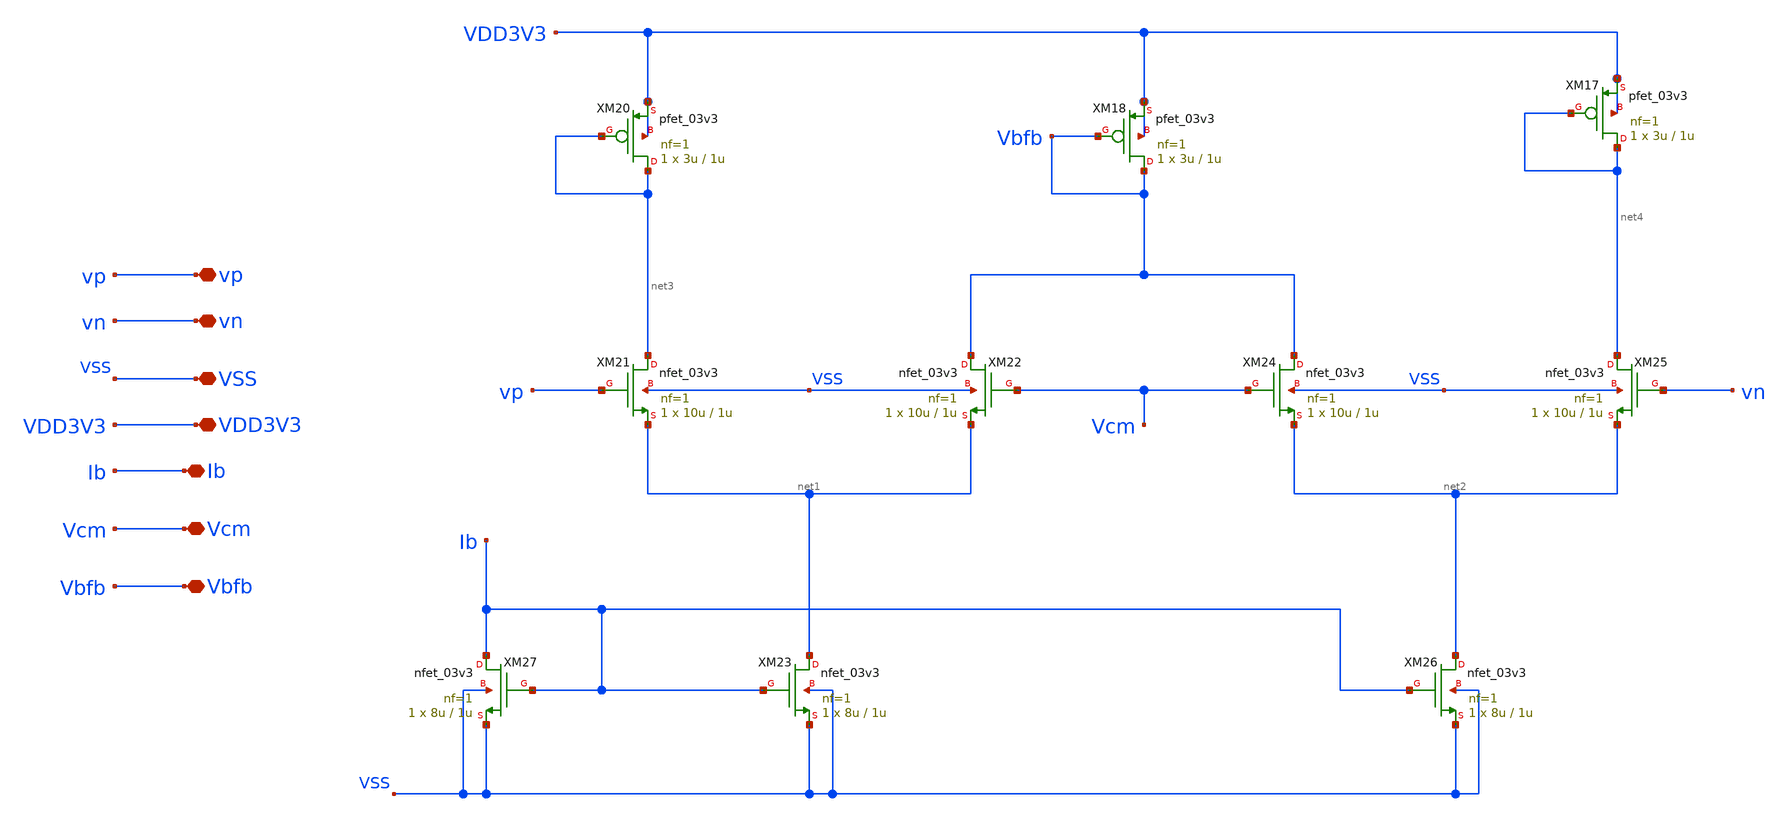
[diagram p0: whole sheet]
** sch_path: designs/libs/core_pga/folded_cascode/cmfb.sch
**.subckt cmfb VSS VDD3V3 Ib Vcm Vbfb vp vn
*.iopin VSS
*.iopin VDD3V3
*.iopin Ib
*.iopin Vcm
*.iopin Vbfb
*.iopin vp
*.iopin vn
XM20 net3 net3 VDD3V3 VDD3V3 pfet_03v3 L=1u W=3u nf=1 ad='int((nf+1)/2) * W/nf * 0.18u' as='int((nf+2)/2) * W/nf * 0.18u'
+ pd='2*int((nf+1)/2) * (W/nf + 0.18u)' ps='2*int((nf+2)/2) * (W/nf + 0.18u)' nrd='0.18u / W' nrs='0.18u / W'
+ sa=0 sb=0 sd=0 m=1
XM21 net3 vp net1 VSS nfet_03v3 L=1u W=10u nf=1 ad='int((nf+1)/2) * W/nf * 0.18u' as='int((nf+2)/2) * W/nf * 0.18u'
+ pd='2*int((nf+1)/2) * (W/nf + 0.18u)' ps='2*int((nf+2)/2) * (W/nf + 0.18u)' nrd='0.18u / W' nrs='0.18u / W'
+ sa=0 sb=0 sd=0 m=1
XM22 Vbfb Vcm net1 VSS nfet_03v3 L=1u W=10u nf=1 ad='int((nf+1)/2) * W/nf * 0.18u' as='int((nf+2)/2) * W/nf * 0.18u'
+ pd='2*int((nf+1)/2) * (W/nf + 0.18u)' ps='2*int((nf+2)/2) * (W/nf + 0.18u)' nrd='0.18u / W' nrs='0.18u / W'
+ sa=0 sb=0 sd=0 m=1
XM23 net1 Ib VSS VSS nfet_03v3 L=1u W=8u nf=1 ad='int((nf+1)/2) * W/nf * 0.18u' as='int((nf+2)/2) * W/nf * 0.18u'
+ pd='2*int((nf+1)/2) * (W/nf + 0.18u)' ps='2*int((nf+2)/2) * (W/nf + 0.18u)' nrd='0.18u / W' nrs='0.18u / W'
+ sa=0 sb=0 sd=0 m=1
XM24 Vbfb Vcm net2 VSS nfet_03v3 L=1u W=10u nf=1 ad='int((nf+1)/2) * W/nf * 0.18u' as='int((nf+2)/2) * W/nf * 0.18u'
+ pd='2*int((nf+1)/2) * (W/nf + 0.18u)' ps='2*int((nf+2)/2) * (W/nf + 0.18u)' nrd='0.18u / W' nrs='0.18u / W'
+ sa=0 sb=0 sd=0 m=1
XM25 net4 vn net2 VSS nfet_03v3 L=1u W=10u nf=1 ad='int((nf+1)/2) * W/nf * 0.18u' as='int((nf+2)/2) * W/nf * 0.18u'
+ pd='2*int((nf+1)/2) * (W/nf + 0.18u)' ps='2*int((nf+2)/2) * (W/nf + 0.18u)' nrd='0.18u / W' nrs='0.18u / W'
+ sa=0 sb=0 sd=0 m=1
XM26 net2 Ib VSS VSS nfet_03v3 L=1u W=8u nf=1 ad='int((nf+1)/2) * W/nf * 0.18u' as='int((nf+2)/2) * W/nf * 0.18u'
+ pd='2*int((nf+1)/2) * (W/nf + 0.18u)' ps='2*int((nf+2)/2) * (W/nf + 0.18u)' nrd='0.18u / W' nrs='0.18u / W'
+ sa=0 sb=0 sd=0 m=1
XM27 Ib Ib VSS VSS nfet_03v3 L=1u W=8u nf=1 ad='int((nf+1)/2) * W/nf * 0.18u' as='int((nf+2)/2) * W/nf * 0.18u'
+ pd='2*int((nf+1)/2) * (W/nf + 0.18u)' ps='2*int((nf+2)/2) * (W/nf + 0.18u)' nrd='0.18u / W' nrs='0.18u / W'
+ sa=0 sb=0 sd=0 m=1
XM17 net4 net4 VDD3V3 VDD3V3 pfet_03v3 L=1u W=3u nf=1 ad='int((nf+1)/2) * W/nf * 0.18u' as='int((nf+2)/2) * W/nf * 0.18u'
+ pd='2*int((nf+1)/2) * (W/nf + 0.18u)' ps='2*int((nf+2)/2) * (W/nf + 0.18u)' nrd='0.18u / W' nrs='0.18u / W'
+ sa=0 sb=0 sd=0 m=1
XM18 Vbfb Vbfb VDD3V3 VDD3V3 pfet_03v3 L=1u W=3u nf=1 ad='int((nf+1)/2) * W/nf * 0.18u' as='int((nf+2)/2) * W/nf * 0.18u'
+ pd='2*int((nf+1)/2) * (W/nf + 0.18u)' ps='2*int((nf+2)/2) * (W/nf + 0.18u)' nrd='0.18u / W' nrs='0.18u / W'
+ sa=0 sb=0 sd=0 m=1
**.ends
.end
